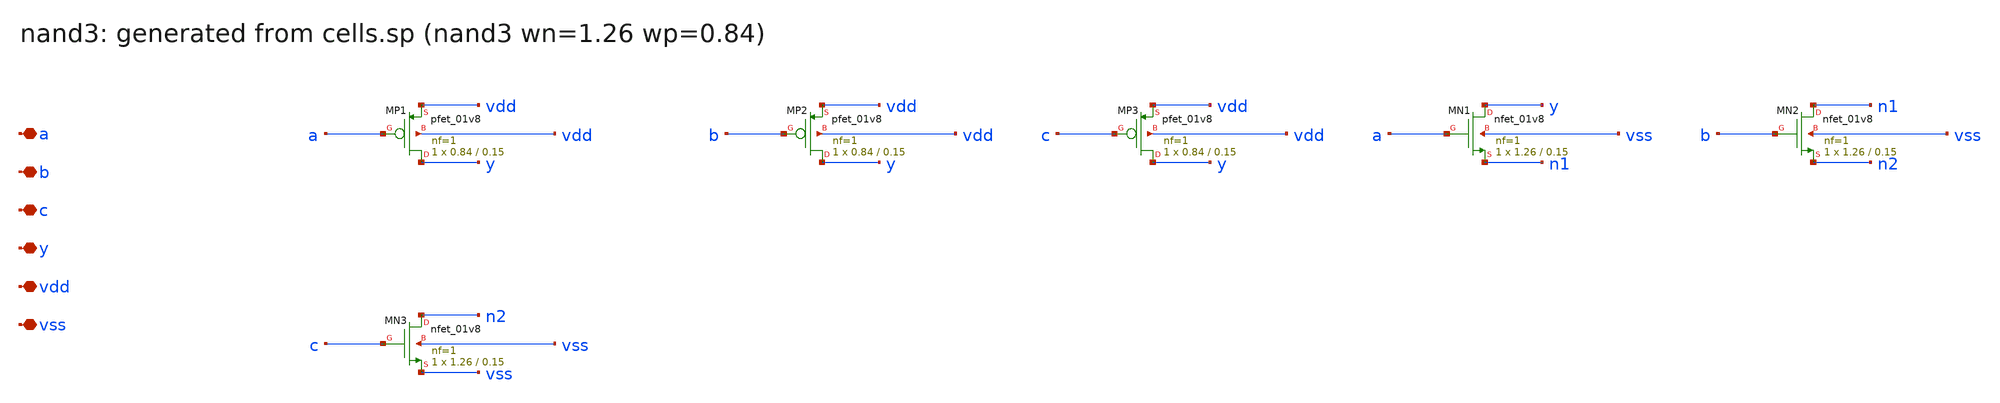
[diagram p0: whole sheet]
** sch_path: sram/xschem/nand3.sch
**.subckt nand3 a b c y vdd vss
*.iopin a
*.iopin b
*.iopin c
*.iopin y
*.iopin vdd
*.iopin vss
XMP1 y a vdd vdd sky130_fd_pr__pfet_01v8 L=0.15 W=0.84 nf=1 ad='int((nf+1)/2) * W/nf * 0.29' as='int((nf+2)/2) * W/nf * 0.29'
+ pd='2*int((nf+1)/2) * (W/nf + 0.29)' ps='2*int((nf+2)/2) * (W/nf + 0.29)' nrd='0.29 / W' nrs='0.29 / W'
+ sa=0 sb=0 sd=0 mult=1 m=1
XMP2 y b vdd vdd sky130_fd_pr__pfet_01v8 L=0.15 W=0.84 nf=1 ad='int((nf+1)/2) * W/nf * 0.29' as='int((nf+2)/2) * W/nf * 0.29'
+ pd='2*int((nf+1)/2) * (W/nf + 0.29)' ps='2*int((nf+2)/2) * (W/nf + 0.29)' nrd='0.29 / W' nrs='0.29 / W'
+ sa=0 sb=0 sd=0 mult=1 m=1
XMP3 y c vdd vdd sky130_fd_pr__pfet_01v8 L=0.15 W=0.84 nf=1 ad='int((nf+1)/2) * W/nf * 0.29' as='int((nf+2)/2) * W/nf * 0.29'
+ pd='2*int((nf+1)/2) * (W/nf + 0.29)' ps='2*int((nf+2)/2) * (W/nf + 0.29)' nrd='0.29 / W' nrs='0.29 / W'
+ sa=0 sb=0 sd=0 mult=1 m=1
XMN1 y a n1 vss sky130_fd_pr__nfet_01v8 L=0.15 W=1.26 nf=1 ad='int((1 + 1)/2) * 1.26 / 1 * 0.29' as='int((1 + 2)/2) * 1.26 / 1 * 0.29'
+ pd='2*int((1 + 1)/2) * (1.26 / 1 + 0.29)' ps='2*int((1 + 2)/2) * (1.26 / 1 + 0.29)' nrd='0.29 / 1.26 '
+ nrs='0.29 / 1.26 ' sa=0 sb=0 sd=0 mult=1 m=1
XMN2 n1 b n2 vss sky130_fd_pr__nfet_01v8 L=0.15 W=1.26 nf=1 ad='int((1 + 1)/2) * 1.26 / 1 * 0.29' as='int((1 + 2)/2) * 1.26 / 1 * 0.29'
+ pd='2*int((1 + 1)/2) * (1.26 / 1 + 0.29)' ps='2*int((1 + 2)/2) * (1.26 / 1 + 0.29)' nrd='0.29 / 1.26 '
+ nrs='0.29 / 1.26 ' sa=0 sb=0 sd=0 mult=1 m=1
XMN3 n2 c vss vss sky130_fd_pr__nfet_01v8 L=0.15 W=1.26 nf=1 ad='int((1 + 1)/2) * 1.26 / 1 * 0.29' as='int((1 + 2)/2) * 1.26 / 1 * 0.29'
+ pd='2*int((1 + 1)/2) * (1.26 / 1 + 0.29)' ps='2*int((1 + 2)/2) * (1.26 / 1 + 0.29)' nrd='0.29 / 1.26 '
+ nrs='0.29 / 1.26 ' sa=0 sb=0 sd=0 mult=1 m=1
**.ends
.end
